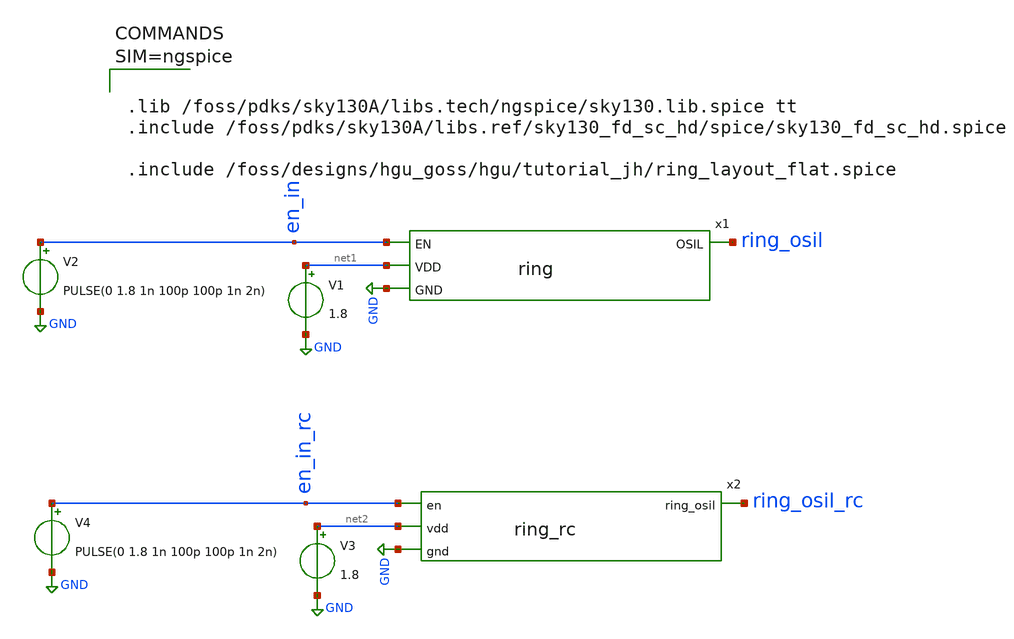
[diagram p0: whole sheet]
** sch_path: hgu/tutorial_jh/tb_ring.sch
**.subckt tb_ring
x1 ring_osil en_in net1 GND ring
V1 net1 GND 1.8
V2 en_in GND PULSE(0 1.8 1n 100p 100p 1n 2n)
V3 net2 GND 1.8
V4 en_in_rc GND PULSE(0 1.8 1n 100p 100p 1n 2n)
x2 en_in_rc ring_osil_rc net2 GND ring_rc
**** begin user architecture code


.tran 1p 10n
.save all
.control
	option temp = 100
	run
	plot ring_osil en_in
	plot ring_osil_rc en_in_rc
.endc





.lib /foss/pdks/sky130A/libs.tech/ngspice/sky130.lib.spice tt
.include /foss/pdks/sky130A/libs.ref/sky130_fd_sc_hd/spice/sky130_fd_sc_hd.spice

.include /foss/designs/hgu_goss/hgu/tutorial_jh/ring_layout_flat.spice



**** end user architecture code
**.ends

* expanding   symbol:  /foss/designs/hgu_goss/hgu/tutorial_jh/ring.sym # of pins=4
** sym_path: hgu/tutorial_jh/ring.sym
** sch_path: hgu/tutorial_jh/ring.sch
.subckt ring OSIL EN VDD GND
*.ipin EN
*.opin OSIL
*.ipin GND
*.ipin VDD
x1 net1 GND GND VDD VDD net2 sky130_fd_sc_hd__inv_1
x5 EN OSIL GND GND VDD VDD net1 sky130_fd_sc_hd__nand2_1
x2 net2 GND GND VDD VDD net3 sky130_fd_sc_hd__inv_1
x3 net3 GND GND VDD VDD net4 sky130_fd_sc_hd__inv_1
x4 net4 GND GND VDD VDD OSIL sky130_fd_sc_hd__inv_1
.ends

.GLOBAL GND
.end
